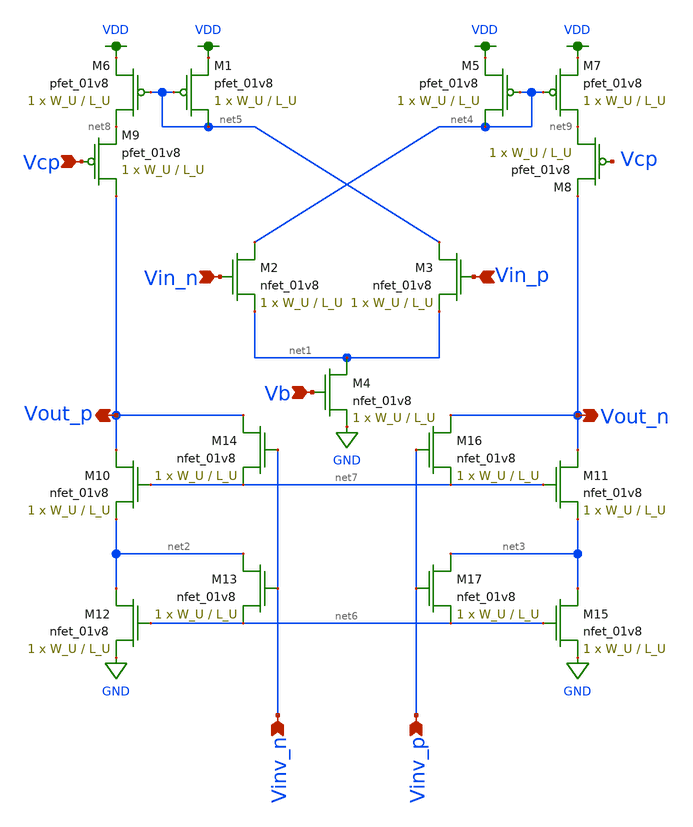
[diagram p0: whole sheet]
** sch_path: schematics/OTA.sch
**.subckt OTA Vcp Vb Vinv_n Vinv_p Vin_n Vin_p Vout_n Vout_p
*.ipin Vcp
*.ipin Vb
*.ipin Vinv_n
*.ipin Vinv_p
*.ipin Vin_n
*.ipin Vin_p
*.opin Vout_n
*.opin Vout_p
XM1 net5 net5 VDD VDD sky130_fd_pr__pfet_01v8 L=L_U W=W_U nf=1 ad='int((nf+1)/2) * W/nf * 0.29' as='int((nf+2)/2) * W/nf * 0.29'
+ pd='2*int((nf+1)/2) * (W/nf + 0.29)' ps='2*int((nf+2)/2) * (W/nf + 0.29)' nrd='0.29 / W' nrs='0.29 / W'
+ sa=0 sb=0 sd=0 mult=1 m=1
XM2 net4 Vin_n net1 GND sky130_fd_pr__nfet_01v8 L=L_U W=W_U nf=1 ad='int((nf+1)/2) * W/nf * 0.29' as='int((nf+2)/2) * W/nf * 0.29'
+ pd='2*int((nf+1)/2) * (W/nf + 0.29)' ps='2*int((nf+2)/2) * (W/nf + 0.29)' nrd='0.29 / W' nrs='0.29 / W'
+ sa=0 sb=0 sd=0 mult=1 m=1
XM3 net5 Vin_p net1 GND sky130_fd_pr__nfet_01v8 L=L_U W=W_U nf=1 ad='int((nf+1)/2) * W/nf * 0.29' as='int((nf+2)/2) * W/nf * 0.29'
+ pd='2*int((nf+1)/2) * (W/nf + 0.29)' ps='2*int((nf+2)/2) * (W/nf + 0.29)' nrd='0.29 / W' nrs='0.29 / W'
+ sa=0 sb=0 sd=0 mult=1 m=1
XM4 net1 Vb GND GND sky130_fd_pr__nfet_01v8 L=L_U W=W_U nf=1 ad='int((nf+1)/2) * W/nf * 0.29' as='int((nf+2)/2) * W/nf * 0.29'
+ pd='2*int((nf+1)/2) * (W/nf + 0.29)' ps='2*int((nf+2)/2) * (W/nf + 0.29)' nrd='0.29 / W' nrs='0.29 / W'
+ sa=0 sb=0 sd=0 mult=1 m=1
XM5 net4 net4 VDD VDD sky130_fd_pr__pfet_01v8 L=L_U W=W_U nf=1 ad='int((nf+1)/2) * W/nf * 0.29' as='int((nf+2)/2) * W/nf * 0.29'
+ pd='2*int((nf+1)/2) * (W/nf + 0.29)' ps='2*int((nf+2)/2) * (W/nf + 0.29)' nrd='0.29 / W' nrs='0.29 / W'
+ sa=0 sb=0 sd=0 mult=1 m=1
XM6 net8 net5 VDD VDD sky130_fd_pr__pfet_01v8 L=L_U W=W_U nf=1 ad='int((nf+1)/2) * W/nf * 0.29' as='int((nf+2)/2) * W/nf * 0.29'
+ pd='2*int((nf+1)/2) * (W/nf + 0.29)' ps='2*int((nf+2)/2) * (W/nf + 0.29)' nrd='0.29 / W' nrs='0.29 / W'
+ sa=0 sb=0 sd=0 mult=1 m=1
XM7 net9 net4 VDD VDD sky130_fd_pr__pfet_01v8 L=L_U W=W_U nf=1 ad='int((nf+1)/2) * W/nf * 0.29' as='int((nf+2)/2) * W/nf * 0.29'
+ pd='2*int((nf+1)/2) * (W/nf + 0.29)' ps='2*int((nf+2)/2) * (W/nf + 0.29)' nrd='0.29 / W' nrs='0.29 / W'
+ sa=0 sb=0 sd=0 mult=1 m=1
XM8 net9 Vcp Vout_n VDD sky130_fd_pr__pfet_01v8 L=L_U W=W_U nf=1 ad='int((nf+1)/2) * W/nf * 0.29' as='int((nf+2)/2) * W/nf * 0.29'
+ pd='2*int((nf+1)/2) * (W/nf + 0.29)' ps='2*int((nf+2)/2) * (W/nf + 0.29)' nrd='0.29 / W' nrs='0.29 / W'
+ sa=0 sb=0 sd=0 mult=1 m=1
XM9 Vout_p Vcp net8 VDD sky130_fd_pr__pfet_01v8 L=L_U W=W_U nf=1 ad='int((nf+1)/2) * W/nf * 0.29' as='int((nf+2)/2) * W/nf * 0.29'
+ pd='2*int((nf+1)/2) * (W/nf + 0.29)' ps='2*int((nf+2)/2) * (W/nf + 0.29)' nrd='0.29 / W' nrs='0.29 / W'
+ sa=0 sb=0 sd=0 mult=1 m=1
XM10 Vout_p net7 net2 GND sky130_fd_pr__nfet_01v8 L=L_U W=W_U nf=1 ad='int((nf+1)/2) * W/nf * 0.29' as='int((nf+2)/2) * W/nf * 0.29'
+ pd='2*int((nf+1)/2) * (W/nf + 0.29)' ps='2*int((nf+2)/2) * (W/nf + 0.29)' nrd='0.29 / W' nrs='0.29 / W'
+ sa=0 sb=0 sd=0 mult=1 m=1
XM11 Vout_n net7 net3 GND sky130_fd_pr__nfet_01v8 L=L_U W=W_U nf=1 ad='int((nf+1)/2) * W/nf * 0.29' as='int((nf+2)/2) * W/nf * 0.29'
+ pd='2*int((nf+1)/2) * (W/nf + 0.29)' ps='2*int((nf+2)/2) * (W/nf + 0.29)' nrd='0.29 / W' nrs='0.29 / W'
+ sa=0 sb=0 sd=0 mult=1 m=1
XM12 net2 net6 GND GND sky130_fd_pr__nfet_01v8 L=L_U W=W_U nf=1 ad='int((nf+1)/2) * W/nf * 0.29' as='int((nf+2)/2) * W/nf * 0.29'
+ pd='2*int((nf+1)/2) * (W/nf + 0.29)' ps='2*int((nf+2)/2) * (W/nf + 0.29)' nrd='0.29 / W' nrs='0.29 / W'
+ sa=0 sb=0 sd=0 mult=1 m=1
XM13 net2 Vinv_n net6 GND sky130_fd_pr__nfet_01v8 L=L_U W=W_U nf=1 ad='int((nf+1)/2) * W/nf * 0.29' as='int((nf+2)/2) * W/nf * 0.29'
+ pd='2*int((nf+1)/2) * (W/nf + 0.29)' ps='2*int((nf+2)/2) * (W/nf + 0.29)' nrd='0.29 / W' nrs='0.29 / W'
+ sa=0 sb=0 sd=0 mult=1 m=1
XM14 Vout_p Vinv_n net7 GND sky130_fd_pr__nfet_01v8 L=L_U W=W_U nf=1 ad='int((nf+1)/2) * W/nf * 0.29'
+ as='int((nf+2)/2) * W/nf * 0.29' pd='2*int((nf+1)/2) * (W/nf + 0.29)' ps='2*int((nf+2)/2) * (W/nf + 0.29)'
+ nrd='0.29 / W' nrs='0.29 / W' sa=0 sb=0 sd=0 mult=1 m=1
XM15 net3 net6 GND GND sky130_fd_pr__nfet_01v8 L=L_U W=W_U nf=1 ad='int((nf+1)/2) * W/nf * 0.29' as='int((nf+2)/2) * W/nf * 0.29'
+ pd='2*int((nf+1)/2) * (W/nf + 0.29)' ps='2*int((nf+2)/2) * (W/nf + 0.29)' nrd='0.29 / W' nrs='0.29 / W'
+ sa=0 sb=0 sd=0 mult=1 m=1
XM16 Vout_n Vinv_p net7 GND sky130_fd_pr__nfet_01v8 L=L_U W=W_U nf=1 ad='int((nf+1)/2) * W/nf * 0.29'
+ as='int((nf+2)/2) * W/nf * 0.29' pd='2*int((nf+1)/2) * (W/nf + 0.29)' ps='2*int((nf+2)/2) * (W/nf + 0.29)'
+ nrd='0.29 / W' nrs='0.29 / W' sa=0 sb=0 sd=0 mult=1 m=1
XM17 net3 Vinv_p net6 GND sky130_fd_pr__nfet_01v8 L=L_U W=W_U nf=1 ad='int((nf+1)/2) * W/nf * 0.29' as='int((nf+2)/2) * W/nf * 0.29'
+ pd='2*int((nf+1)/2) * (W/nf + 0.29)' ps='2*int((nf+2)/2) * (W/nf + 0.29)' nrd='0.29 / W' nrs='0.29 / W'
+ sa=0 sb=0 sd=0 mult=1 m=1
**.ends
.GLOBAL VDD
.GLOBAL GND
.end
